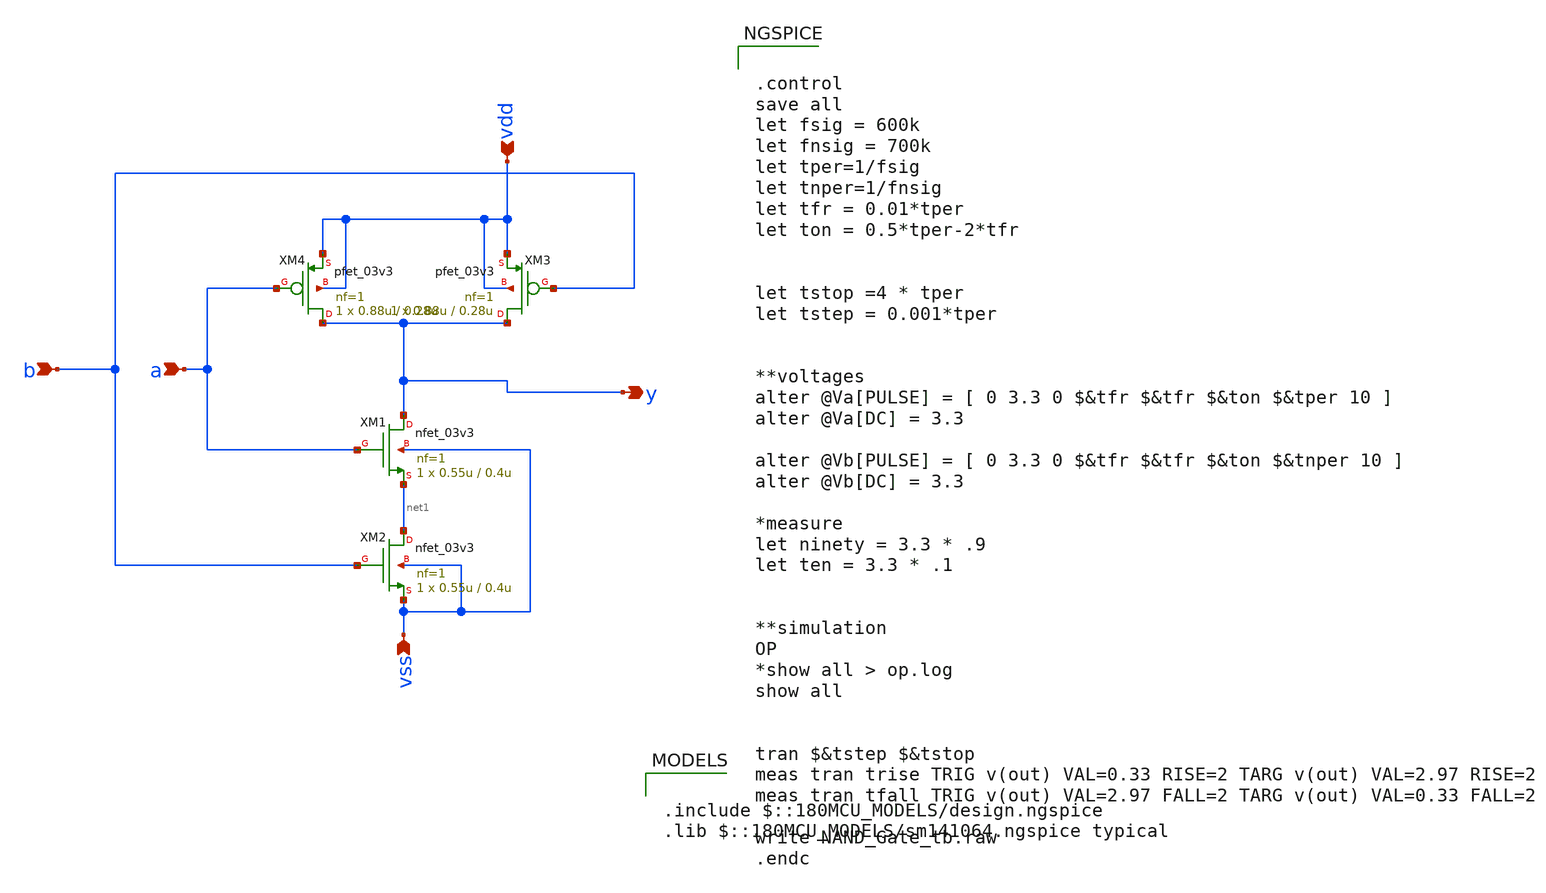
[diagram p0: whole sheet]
** sch_path: designs/libs/core_analog/op_Gates/NAND_Gate.sch
**.subckt NAND_Gate b a vss vdd y
*.ipin b
*.ipin a
*.ipin vss
*.ipin vdd
*.opin y
XM1 y a net1 vss nfet_03v3 L=0.4u W=0.55u nf=1 ad='int((nf+1)/2) * W/nf * 0.18u' as='int((nf+2)/2) * W/nf * 0.18u'
+ pd='2*int((nf+1)/2) * (W/nf + 0.18u)' ps='2*int((nf+2)/2) * (W/nf + 0.18u)' nrd='0.18u / W' nrs='0.18u / W'
+ sa=0 sb=0 sd=0 m=1
XM2 net1 b vss vss nfet_03v3 L=0.4u W=0.55u nf=1 ad='int((nf+1)/2) * W/nf * 0.18u' as='int((nf+2)/2) * W/nf * 0.18u'
+ pd='2*int((nf+1)/2) * (W/nf + 0.18u)' ps='2*int((nf+2)/2) * (W/nf + 0.18u)' nrd='0.18u / W' nrs='0.18u / W'
+ sa=0 sb=0 sd=0 m=1
XM3 y b vdd vdd pfet_03v3 L=0.28u W=0.88u nf=1 ad='int((nf+1)/2) * W/nf * 0.18u' as='int((nf+2)/2) * W/nf * 0.18u'
+ pd='2*int((nf+1)/2) * (W/nf + 0.18u)' ps='2*int((nf+2)/2) * (W/nf + 0.18u)' nrd='0.18u / W' nrs='0.18u / W'
+ sa=0 sb=0 sd=0 m=1
XM4 y a vdd vdd pfet_03v3 L=0.28u W=0.88u nf=1 ad='int((nf+1)/2) * W/nf * 0.18u' as='int((nf+2)/2) * W/nf * 0.18u'
+ pd='2*int((nf+1)/2) * (W/nf + 0.18u)' ps='2*int((nf+2)/2) * (W/nf + 0.18u)' nrd='0.18u / W' nrs='0.18u / W'
+ sa=0 sb=0 sd=0 m=1
**** begin user architecture code


.control
save all
let fsig = 600k
let fnsig = 700k
let tper=1/fsig
let tnper=1/fnsig
let tfr = 0.01*tper
let ton = 0.5*tper-2*tfr


let tstop =4 * tper
let tstep = 0.001*tper


**voltages
alter @Va[PULSE] = [ 0 3.3 0 $&tfr $&tfr $&ton $&tper 10 ]
alter @Va[DC] = 3.3

alter @Vb[PULSE] = [ 0 3.3 0 $&tfr $&tfr $&ton $&tnper 10 ]
alter @Vb[DC] = 3.3

*measure
let ninety = 3.3 * .9
let ten = 3.3 * .1


**simulation
OP
*show all > op.log
show all


tran $&tstep $&tstop
meas tran trise TRIG v(out) VAL=0.33 RISE=2 TARG v(out) VAL=2.97 RISE=2
meas tran tfall TRIG v(out) VAL=2.97 FALL=2 TARG v(out) VAL=0.33 FALL=2

write NAND_Gate_tb.raw
.endc



.include $::180MCU_MODELS/design.ngspice
.lib $::180MCU_MODELS/sm141064.ngspice typical

**** end user architecture code
**.ends
.end
